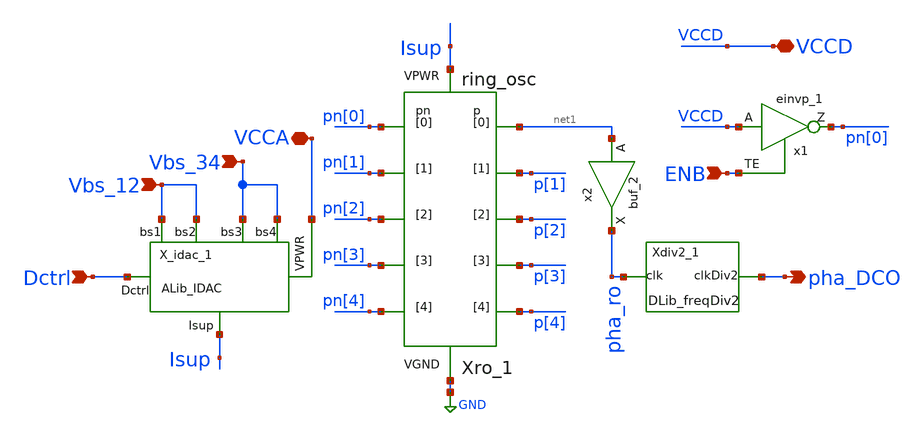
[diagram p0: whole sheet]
** sch_path: xschem/lib/ALib_DCO.sch
**.subckt ALib_DCO Dctrl Vbs_12 Vbs_34 VCCA pha_DCO VCCD ENB
*.ipin Dctrl
*.ipin Vbs_12
*.ipin Vbs_34
*.iopin VCCA
*.opin pha_DCO
*.iopin VCCD
*.ipin ENB
x1 VCCD ENB VGND VNB VPB VPWR pn[0] sky130_fd_sc_hd__einvp_1
Xro_1 GND Isup net1 p[1] p[2] p[3] p[4] pn[0] pn[1] pn[2] pn[3] pn[4] ring_osc L12="L12" Wp12="Wp12"
+ Wn12="Wn12" L34="L34" Wp34="Wp34" Wn34="Wn34"
X_idac_1 Dctrl Vbs_12 Vbs_12 Vbs_34 Vbs_34 VCCA Isup ALib_IDAC W_br1="W_br1" L_br1="L_br1"
+ W_br2="W_br2" L_br2="L_br2" Wp_lk="Wp_lk" Lp_lk="Lp_lk" Wn_lk="Wn_lk" Ln_lk="Wn_lk"
x2 net1 GND GND VCCD VCCD pha_ro sky130_fd_sc_hd__buf_2
Xdiv2_1 pha_ro GND GND VCCD VCCD pha_DCO DLib_freqDiv2
**.ends
.GLOBAL GND
.end
